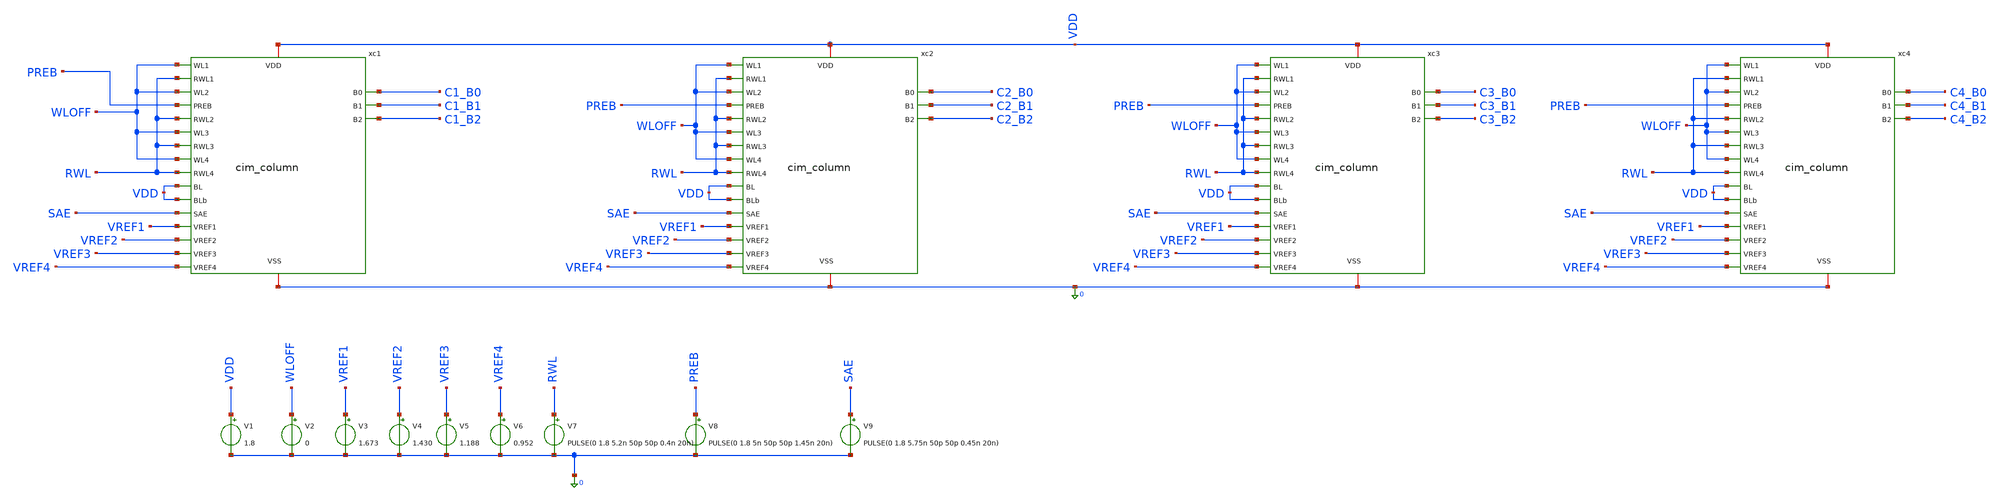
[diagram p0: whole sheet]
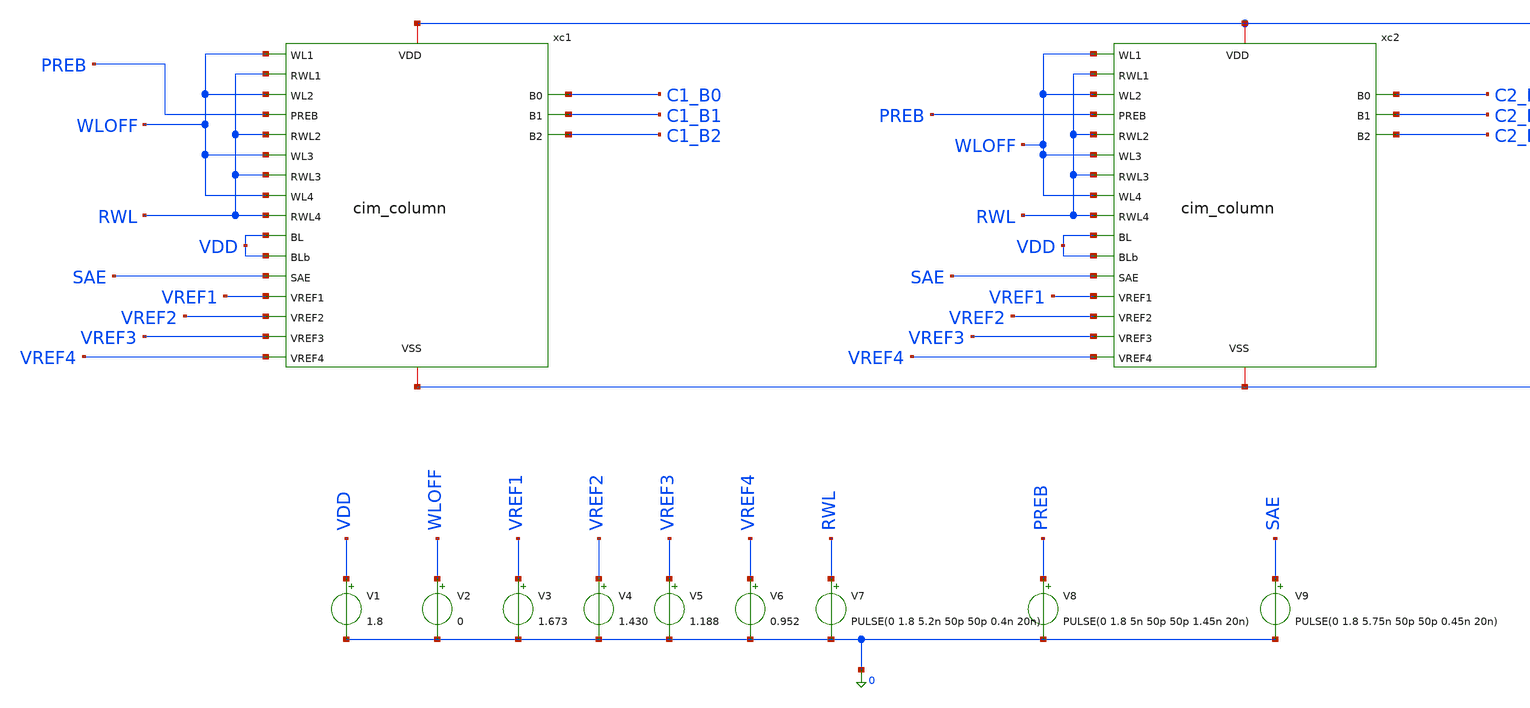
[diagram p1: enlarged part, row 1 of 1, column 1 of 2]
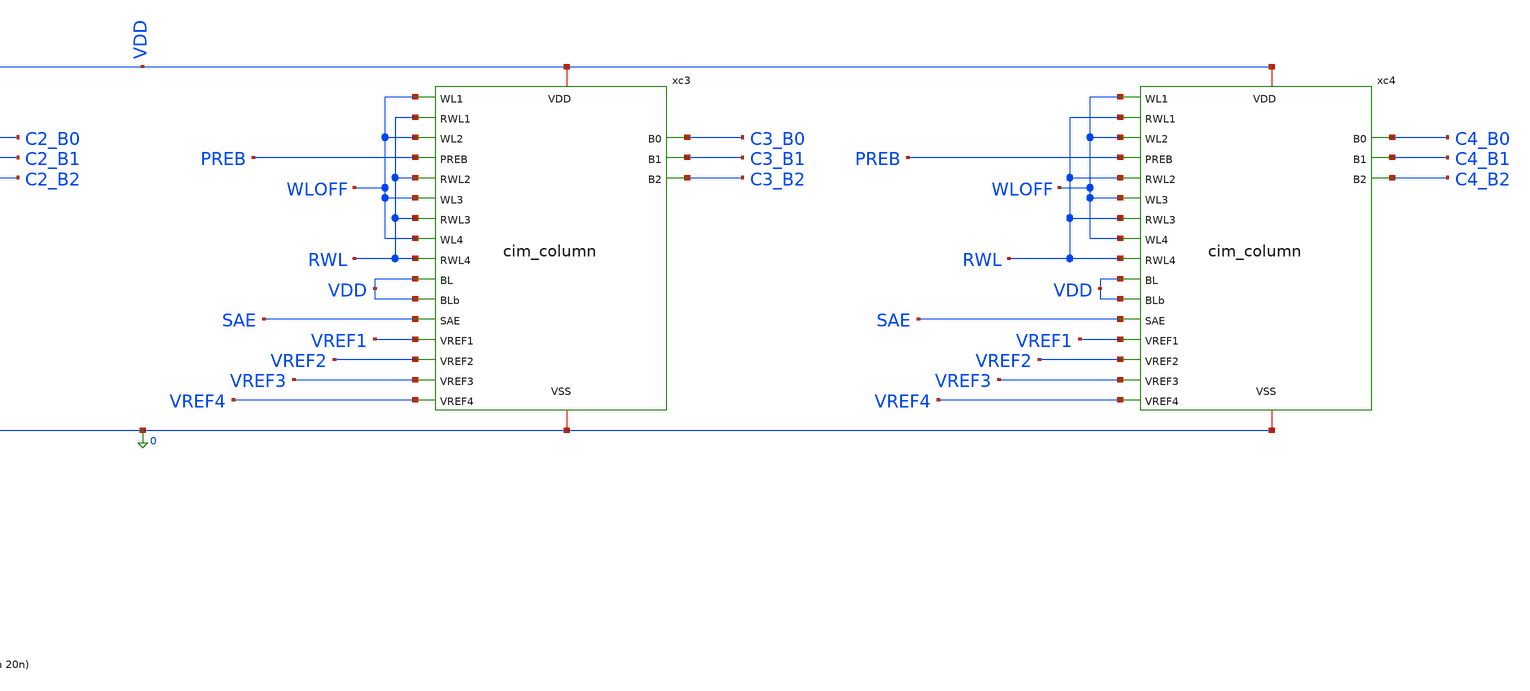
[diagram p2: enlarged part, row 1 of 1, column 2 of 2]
** sch_path: schematics/cim_array4x4_tb.sch
**.subckt cim_array4x4_tb
xc1 VDD WLOFF RWL WLOFF PREB RWL WLOFF RWL WLOFF RWL 0 VDD VDD SAE VREF1 C1_B0 VREF2 C1_B1 VREF3
+ C1_B2 VREF4 cim_column
xc2 VDD WLOFF RWL WLOFF PREB RWL WLOFF RWL WLOFF RWL 0 VDD VDD SAE VREF1 C2_B0 VREF2 C2_B1 VREF3
+ C2_B2 VREF4 cim_column
xc3 VDD WLOFF RWL WLOFF PREB RWL WLOFF RWL WLOFF RWL 0 VDD VDD SAE VREF1 C3_B0 VREF2 C3_B1 VREF3
+ C3_B2 VREF4 cim_column
xc4 VDD WLOFF RWL WLOFF PREB RWL WLOFF RWL WLOFF RWL 0 VDD VDD SAE VREF1 C4_B0 VREF2 C4_B1 VREF3
+ C4_B2 VREF4 cim_column
V1 VDD 0 1.8
V2 WLOFF 0 0
V3 VREF1 0 1.673
V4 VREF2 0 1.430
V5 VREF3 0 1.188
V6 VREF4 0 0.952
V7 RWL 0 PULSE(0 1.8 5.2n 50p 50p 0.4n 20n)
V8 PREB 0 PULSE(0 1.8 5n 50p 50p 1.45n 20n)
V9 SAE 0 PULSE(0 1.8 5.75n 50p 50p 0.45n 20n)
**** begin user architecture code


.lib /usr/local/share/pdk/sky130A/libs.tech/ngspice/sky130.lib.spice tt
.ic v(xc1.xcol.x1.q)=1.8 v(xc1.xcol.x1.qb)=0 v(xc1.xcol.x2.q)=0 v(xc1.xcol.x2.qb)=1.8
+ v(xc1.xcol.x3.q)=0 v(xc1.xcol.x3.qb)=1.8 v(xc1.xcol.x4.q)=0 v(xc1.xcol.x4.qb)=1.8 v(xc2.xcol.x1.q)=1.8
+ v(xc2.xcol.x1.qb)=0 v(xc2.xcol.x2.q)=1.8 v(xc2.xcol.x2.qb)=0 v(xc2.xcol.x3.q)=0 v(xc2.xcol.x3.qb)=1.8
+ v(xc2.xcol.x4.q)=0 v(xc2.xcol.x4.qb)=1.8 v(xc3.xcol.x1.q)=1.8 v(xc3.xcol.x1.qb)=0 v(xc3.xcol.x2.q)=1.8
+ v(xc3.xcol.x2.qb)=0 v(xc3.xcol.x3.q)=1.8 v(xc3.xcol.x3.qb)=0 v(xc3.xcol.x4.q)=0 v(xc3.xcol.x4.qb)=1.8
+ v(xc4.xcol.x1.q)=1.8 v(xc4.xcol.x1.qb)=0 v(xc4.xcol.x2.q)=1.8 v(xc4.xcol.x2.qb)=0 v(xc4.xcol.x3.q)=1.8
+ v(xc4.xcol.x3.qb)=0 v(xc4.xcol.x4.q)=1.8 v(xc4.xcol.x4.qb)=0
.tran 5p 10n uic
.control
run
meas tran c1_b2 FIND v(c1_b2) AT=9n
meas tran c1_b1 FIND v(c1_b1) AT=9n
meas tran c1_b0 FIND v(c1_b0) AT=9n
meas tran c2_b2 FIND v(c2_b2) AT=9n
meas tran c2_b1 FIND v(c2_b1) AT=9n
meas tran c2_b0 FIND v(c2_b0) AT=9n
meas tran c3_b2 FIND v(c3_b2) AT=9n
meas tran c3_b1 FIND v(c3_b1) AT=9n
meas tran c3_b0 FIND v(c3_b0) AT=9n
meas tran c4_b2 FIND v(c4_b2) AT=9n
meas tran c4_b1 FIND v(c4_b1) AT=9n
meas tran c4_b0 FIND v(c4_b0) AT=9n
plot v(xc1.rbl) v(xc2.rbl) v(xc3.rbl) v(xc4.rbl)
.endc


**** end user architecture code
**.ends
.end
